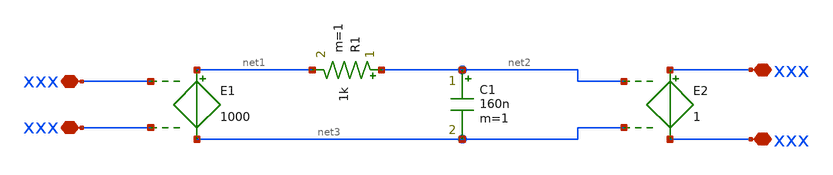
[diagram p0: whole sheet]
** sch_path: xschem/0pa_mod2.sch
**.subckt 0pa_mod2 xxx xxx xxx xxx
*.iopin xxx
*.iopin xxx
*.iopin xxx
*.iopin xxx
E1 net1 net3 xxx xxx 1000
E2 xxx xxx net2 net3 1
R1 net2 net1 1k m=1
C1 net2 net3 160n m=1
**.ends
.end
